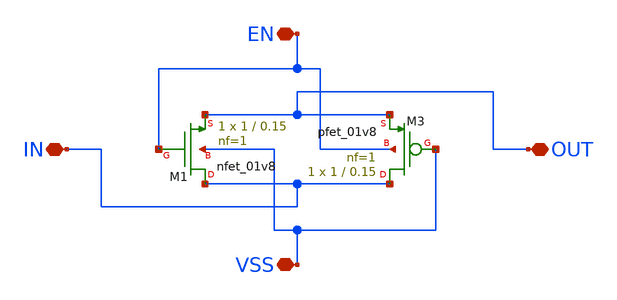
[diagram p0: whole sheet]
** sch_path: npmos_switch.sch
**.subckt npmos_switch EN VSS IN OUT
*.iopin EN
*.iopin VSS
*.iopin IN
*.iopin OUT
XM1 IN EN OUT VSS sky130_fd_pr__nfet_01v8 L=0.15 W=1 nf=1 ad='int((1 + 1)/2) * 1 / 1 * 0.29' as='int((1 + 2)/2) * 1 / 1 * 0.29'
+ pd='2*int((1 + 1)/2) * (1 / 1 + 0.29)' ps='2*int((1 + 2)/2) * (1 / 1 + 0.29)' nrd='0.29 / 1 ' nrs='0.29 / 1 '
+ sa=0 sb=0 sd=0 mult=1 m=1
XM3 IN VSS OUT EN sky130_fd_pr__pfet_01v8 L=0.15 W=1 nf=1 ad='int((nf+1)/2) * W/nf * 0.29' as='int((nf+2)/2) * W/nf * 0.29'
+ pd='2*int((nf+1)/2) * (W/nf + 0.29)' ps='2*int((nf+2)/2) * (W/nf + 0.29)' nrd='0.29 / W' nrs='0.29 / W'
+ sa=0 sb=0 sd=0 mult=1 m=1
**.ends
.end
